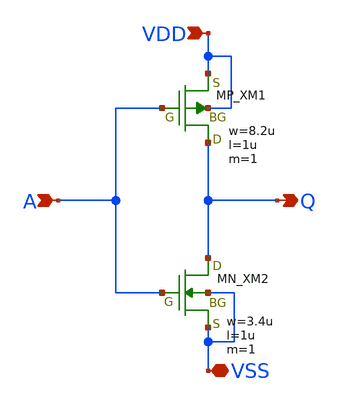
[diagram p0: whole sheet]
** sch_path: member_project/inverter/wipeseals/dist/tr10-inv-wipeseals.sch
**.subckt tr10-inv-wipeseals A Q VSS VDD
*.ipin A
*.opin Q
*.iopin VSS
*.ipin VDD
XM1 Q A VDD VDD PMOS w=8.2u l=1u as=0 ad=0 ps=0 pd=0 nrd=0 nrs=0 m=1
XM2 Q A VSS VSS NMOS w=3.4u l=1u as=0 ad=0 ps=0 pd=0 nrd=0 nrs=0 m=1
**.ends
.end
